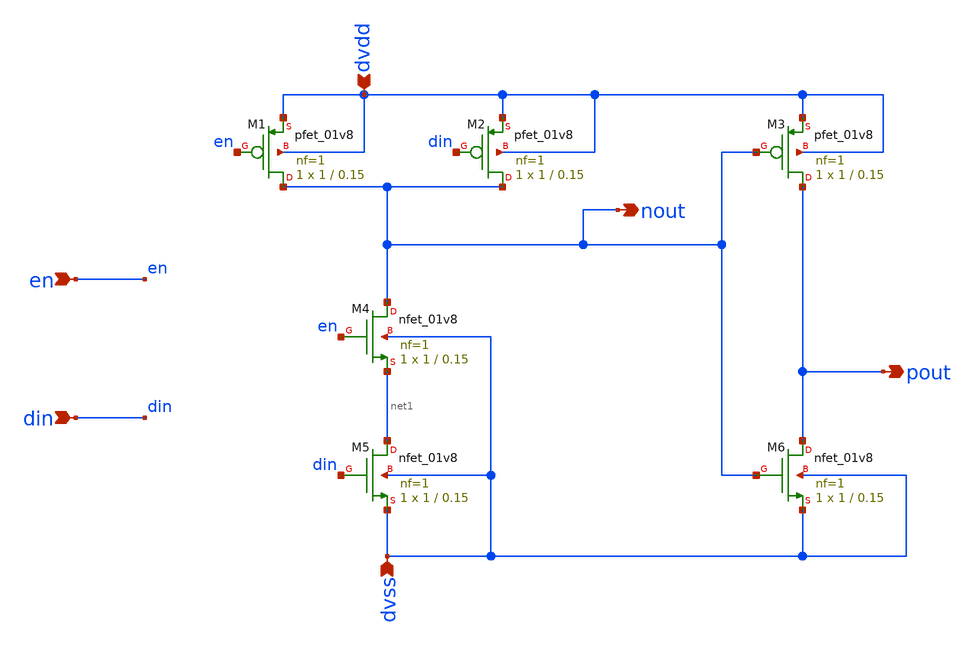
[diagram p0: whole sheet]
** sch_path: xschem/double_output_buffer.sch
**.subckt double_output_buffer din dvdd dvss pout nout en
*.ipin din
*.ipin dvdd
*.ipin dvss
*.opin pout
*.opin nout
*.ipin en
XM1 nout en dvdd dvdd sky130_fd_pr__pfet_01v8 L=0.15 W=1 nf=1 ad='int((nf+1)/2) * W/nf * 0.29' as='int((nf+2)/2) * W/nf * 0.29'
+ pd='2*int((nf+1)/2) * (W/nf + 0.29)' ps='2*int((nf+2)/2) * (W/nf + 0.29)' nrd='0.29 / W' nrs='0.29 / W'
+ sa=0 sb=0 sd=0 mult=1 m=1
XM2 nout din dvdd dvdd sky130_fd_pr__pfet_01v8 L=0.15 W=1 nf=1 ad='int((nf+1)/2) * W/nf * 0.29' as='int((nf+2)/2) * W/nf * 0.29'
+ pd='2*int((nf+1)/2) * (W/nf + 0.29)' ps='2*int((nf+2)/2) * (W/nf + 0.29)' nrd='0.29 / W' nrs='0.29 / W'
+ sa=0 sb=0 sd=0 mult=1 m=1
XM3 pout nout dvdd dvdd sky130_fd_pr__pfet_01v8 L=0.15 W=1 nf=1 ad='int((nf+1)/2) * W/nf * 0.29' as='int((nf+2)/2) * W/nf * 0.29'
+ pd='2*int((nf+1)/2) * (W/nf + 0.29)' ps='2*int((nf+2)/2) * (W/nf + 0.29)' nrd='0.29 / W' nrs='0.29 / W'
+ sa=0 sb=0 sd=0 mult=1 m=1
XM4 nout en net1 dvss sky130_fd_pr__nfet_01v8 L=0.15 W=1 nf=1 ad='int((nf+1)/2) * W/nf * 0.29' as='int((nf+2)/2) * W/nf * 0.29'
+ pd='2*int((nf+1)/2) * (W/nf + 0.29)' ps='2*int((nf+2)/2) * (W/nf + 0.29)' nrd='0.29 / W' nrs='0.29 / W'
+ sa=0 sb=0 sd=0 mult=1 m=1
XM5 net1 din dvss dvss sky130_fd_pr__nfet_01v8 L=0.15 W=1 nf=1 ad='int((nf+1)/2) * W/nf * 0.29' as='int((nf+2)/2) * W/nf * 0.29'
+ pd='2*int((nf+1)/2) * (W/nf + 0.29)' ps='2*int((nf+2)/2) * (W/nf + 0.29)' nrd='0.29 / W' nrs='0.29 / W'
+ sa=0 sb=0 sd=0 mult=1 m=1
XM6 pout nout dvss dvss sky130_fd_pr__nfet_01v8 L=0.15 W=1 nf=1 ad='int((nf+1)/2) * W/nf * 0.29' as='int((nf+2)/2) * W/nf * 0.29'
+ pd='2*int((nf+1)/2) * (W/nf + 0.29)' ps='2*int((nf+2)/2) * (W/nf + 0.29)' nrd='0.29 / W' nrs='0.29 / W'
+ sa=0 sb=0 sd=0 mult=1 m=1
**.ends
.end
